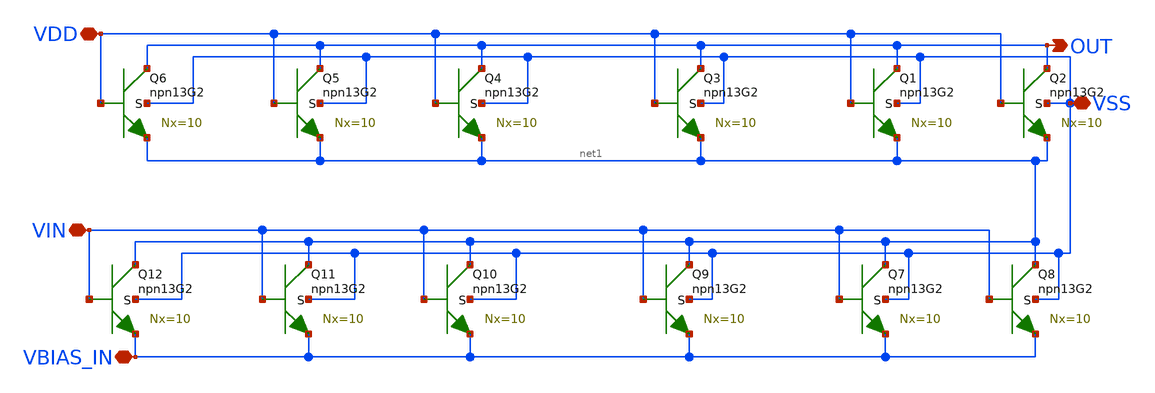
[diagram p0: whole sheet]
** sch_path: GPS_LNA/design_data/lvs/parts/npn_60_2.sch
**.subckt npn_60_2 VSS VIN OUT VDD VBIAS_IN
*.iopin VSS
*.iopin VIN
*.opin OUT
*.iopin VDD
*.iopin VBIAS_IN
XQ1 OUT VDD net1 VSS npn13G2 Nx=10 mm_ok=1
XQ2 OUT VDD net1 VSS npn13G2 Nx=10 mm_ok=1
XQ3 OUT VDD net1 VSS npn13G2 Nx=10 mm_ok=1
XQ4 OUT VDD net1 VSS npn13G2 Nx=10 mm_ok=1
XQ5 OUT VDD net1 VSS npn13G2 Nx=10 mm_ok=1
XQ6 OUT VDD net1 VSS npn13G2 Nx=10 mm_ok=1
XQ7 net1 VIN VBIAS_IN VSS npn13G2 Nx=10 mm_ok=1
XQ8 net1 VIN VBIAS_IN VSS npn13G2 Nx=10 mm_ok=1
XQ9 net1 VIN VBIAS_IN VSS npn13G2 Nx=10 mm_ok=1
XQ10 net1 VIN VBIAS_IN VSS npn13G2 Nx=10 mm_ok=1
XQ11 net1 VIN VBIAS_IN VSS npn13G2 Nx=10 mm_ok=1
XQ12 net1 VIN VBIAS_IN VSS npn13G2 Nx=10 mm_ok=1
**.ends
.end
